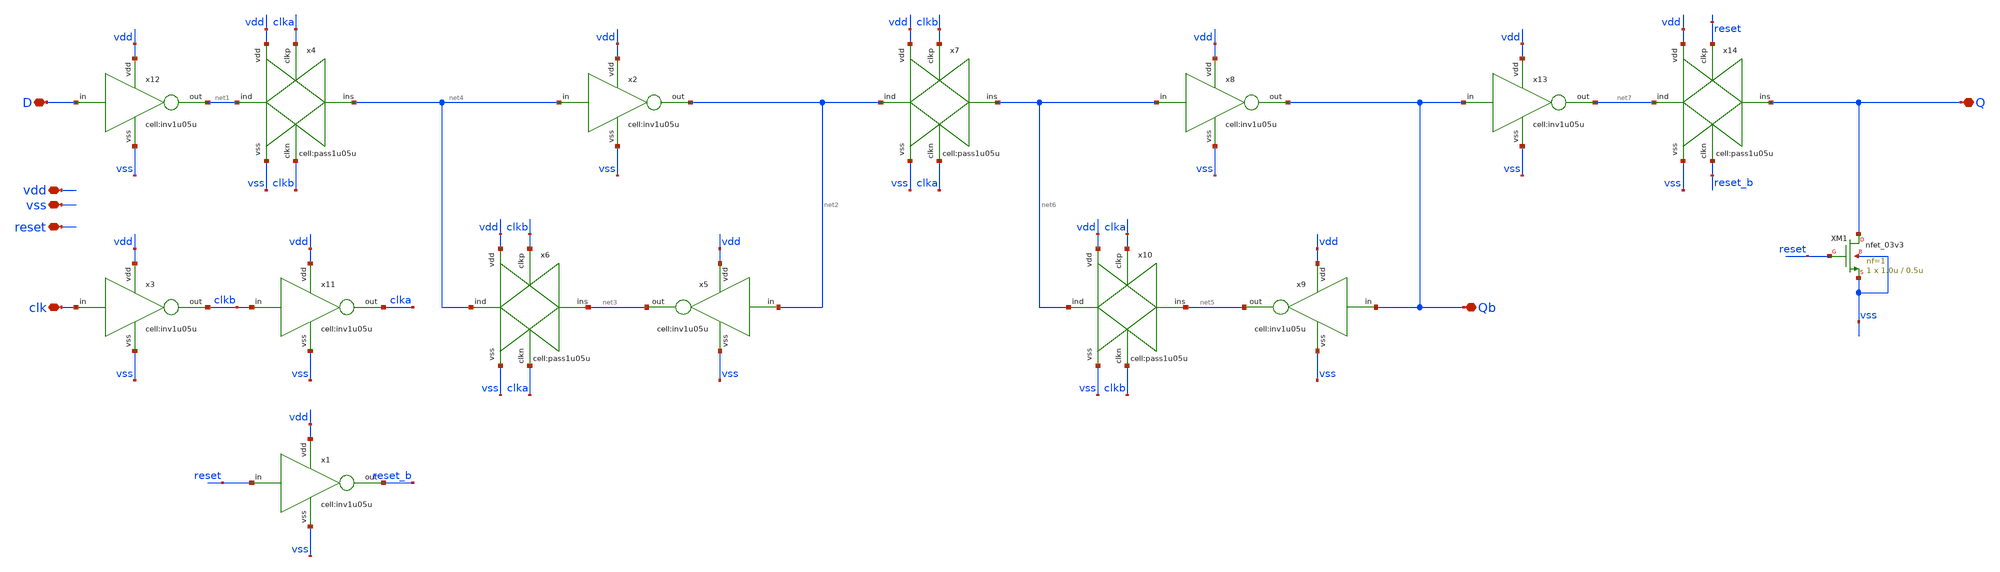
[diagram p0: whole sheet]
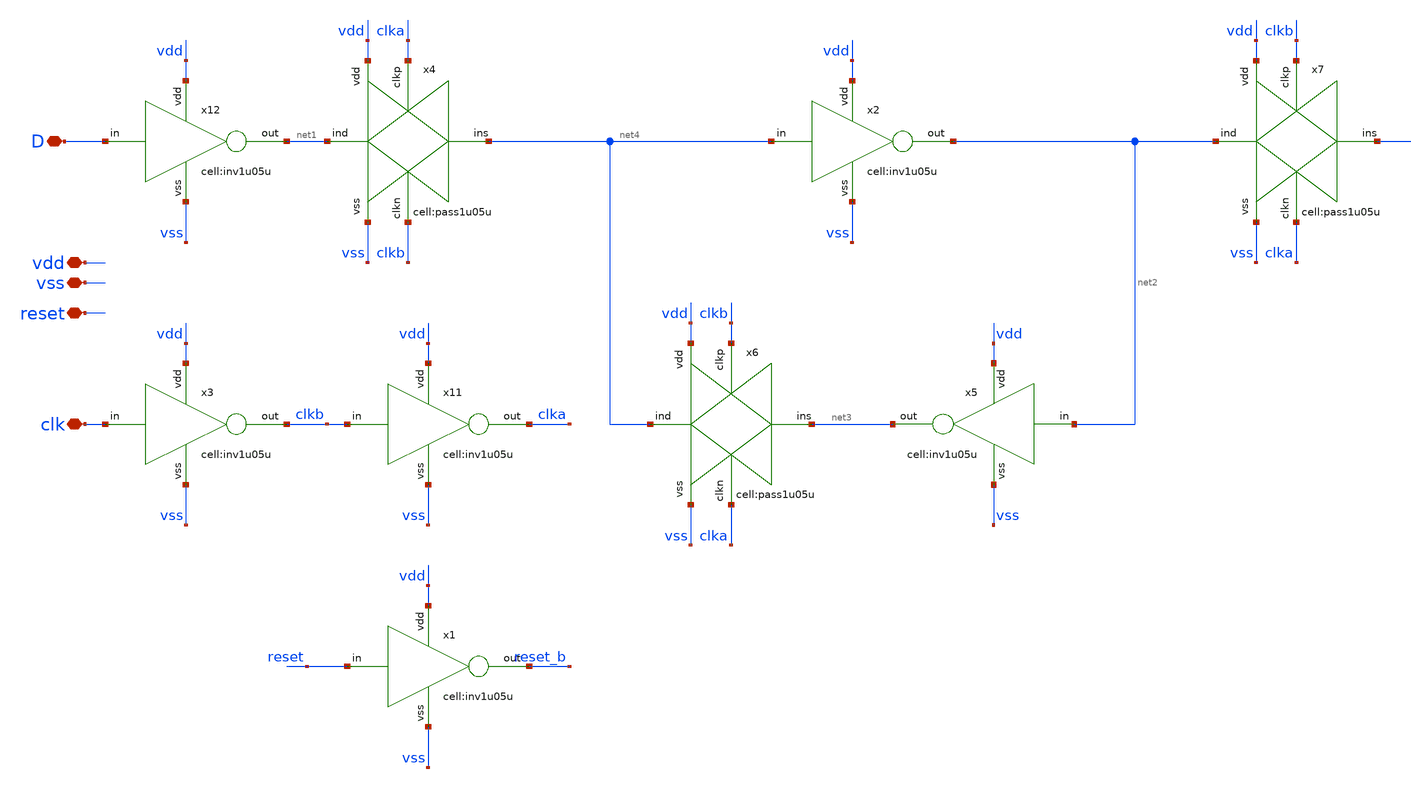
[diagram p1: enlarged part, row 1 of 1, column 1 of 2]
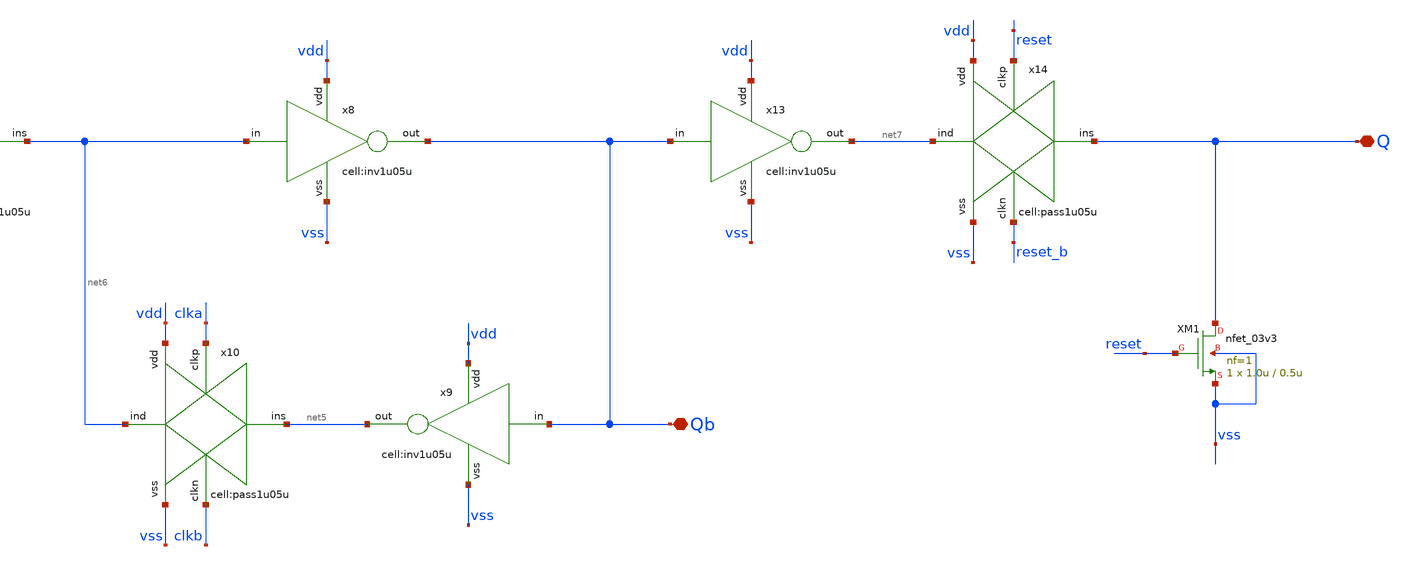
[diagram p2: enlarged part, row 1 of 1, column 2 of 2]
** sch_path: designs/libs/xp_core_analog/qw_DFF_reset/DFF_reset.sch
**.subckt DFF_reset clk vdd vss D Q Qb reset
*.iopin clk
*.iopin vdd
*.iopin vss
*.iopin D
*.iopin Q
*.iopin Qb
*.iopin reset
XM1 Q reset vss vss nfet_03v3 L=0.5u W=1.0u nf=1 ad='int((nf+1)/2) * W/nf * 0.18u' as='int((nf+2)/2) * W/nf * 0.18u'
+ pd='2*int((nf+1)/2) * (W/nf + 0.18u)' ps='2*int((nf+2)/2) * (W/nf + 0.18u)' nrd='0.18u / W' nrs='0.18u / W'
+ sa=0 sb=0 sd=0 m=1
x2 net4 vdd net2 vss inv1u05u
x3 clk vdd clkb vss inv1u05u
x4 net1 vss clkb net4 clka vdd pass1u05u
x5 net2 vdd net3 vss inv1u05u
x6 net4 vss clka net3 clkb vdd pass1u05u
x7 net2 vss clka net6 clkb vdd pass1u05u
x8 net6 vdd Qb vss inv1u05u
x9 Qb vdd net5 vss inv1u05u
x10 net6 vss clkb net5 clka vdd pass1u05u
x11 clkb vdd clka vss inv1u05u
x12 D vdd net1 vss inv1u05u
x13 Qb vdd net7 vss inv1u05u
x1 reset vdd reset_b vss inv1u05u
x14 net7 vss reset_b Q reset vdd pass1u05u
**.ends
.end
